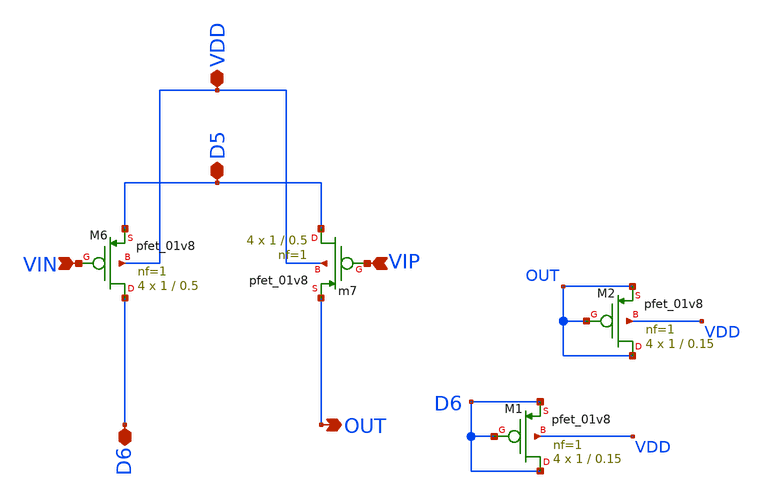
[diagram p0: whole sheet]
** sch_path: opamp/mag/pmos2.sch
**.subckt pmos2 VIN VIP D6 VDD D5 OUT
*.ipin VIN
*.ipin VIP
*.iopin D6
*.iopin VDD
*.iopin D5
*.opin OUT
Xm7 D5 VIP OUT VDD sky130_fd_pr__pfet_01v8 L=0.5 W=1 nf=1 ad='int((nf+1)/2) * W/nf * 0.29' as='int((nf+2)/2) * W/nf * 0.29'
+ pd='2*int((nf+1)/2) * (W/nf + 0.29)' ps='2*int((nf+2)/2) * (W/nf + 0.29)' nrd='0.29 / W' nrs='0.29 / W'
+ sa=0 sb=0 sd=0 mult=4 m=4
XM6 D6 VIN D5 VDD sky130_fd_pr__pfet_01v8 L=0.5 W=1 nf=1 ad='int((nf+1)/2) * W/nf * 0.29' as='int((nf+2)/2) * W/nf * 0.29'
+ pd='2*int((nf+1)/2) * (W/nf + 0.29)' ps='2*int((nf+2)/2) * (W/nf + 0.29)' nrd='0.29 / W' nrs='0.29 / W'
+ sa=0 sb=0 sd=0 mult=4 m=4
XM1 D6 D6 D6 VDD sky130_fd_pr__pfet_01v8 L=0.15 W=1 nf=1 ad='int((nf+1)/2) * W/nf * 0.29' as='int((nf+2)/2) * W/nf * 0.29'
+ pd='2*int((nf+1)/2) * (W/nf + 0.29)' ps='2*int((nf+2)/2) * (W/nf + 0.29)' nrd='0.29 / W' nrs='0.29 / W'
+ sa=0 sb=0 sd=0 mult=4 m=4
XM2 OUT OUT OUT VDD sky130_fd_pr__pfet_01v8 L=0.15 W=1 nf=1 ad='int((nf+1)/2) * W/nf * 0.29' as='int((nf+2)/2) * W/nf * 0.29'
+ pd='2*int((nf+1)/2) * (W/nf + 0.29)' ps='2*int((nf+2)/2) * (W/nf + 0.29)' nrd='0.29 / W' nrs='0.29 / W'
+ sa=0 sb=0 sd=0 mult=4 m=4
**.ends
.end
